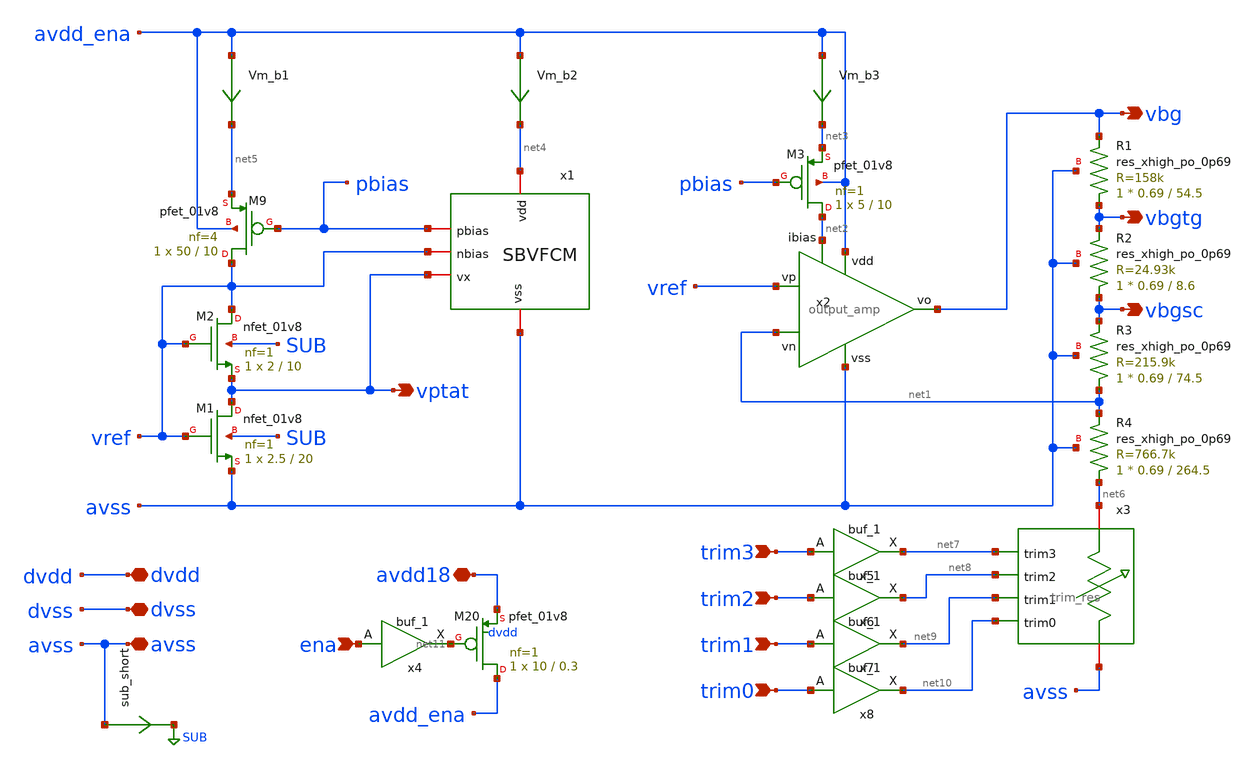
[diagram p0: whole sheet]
** sch_path: xschem/sky130_ak_ip__cmos_vref.sch
**.subckt sky130_ak_ip__cmos_vref vbg avss avdd18 dvdd dvss ena vbgsc vbgtg trim3 trim2 trim1 trim0
*+ vptat
*.opin vbg
*.iopin avss
*.iopin avdd18
*.iopin dvdd
*.iopin dvss
*.ipin ena
*.opin vbgsc
*.opin vbgtg
*.ipin trim3
*.ipin trim2
*.ipin trim1
*.ipin trim0
*.opin vptat
XM2 vref vref vptat SUB sky130_fd_pr__nfet_01v8 L=10 W=2 nf=1 ad='int((nf+1)/2) * W/nf * 0.29' as='int((nf+2)/2) * W/nf * 0.29'
+ pd='2*int((nf+1)/2) * (W/nf + 0.29)' ps='2*int((nf+2)/2) * (W/nf + 0.29)' nrd='0.29 / W' nrs='0.29 / W'
+ sa=0 sb=0 sd=0 mult=1 m=1
XM1 vptat vref avss SUB sky130_fd_pr__nfet_01v8 L=20 W=2.5 nf=1 ad='int((nf+1)/2) * W/nf * 0.29' as='int((nf+2)/2) * W/nf * 0.29'
+ pd='2*int((nf+1)/2) * (W/nf + 0.29)' ps='2*int((nf+2)/2) * (W/nf + 0.29)' nrd='0.29 / W' nrs='0.29 / W'
+ sa=0 sb=0 sd=0 mult=1 m=1
XM9 vref pbias net5 avdd_ena sky130_fd_pr__pfet_01v8 L=10 W=50 nf=4 ad='int((nf+1)/2) * W/nf * 0.29'
+ as='int((nf+2)/2) * W/nf * 0.29' pd='2*int((nf+1)/2) * (W/nf + 0.29)' ps='2*int((nf+2)/2) * (W/nf + 0.29)'
+ nrd='0.29 / W' nrs='0.29 / W' sa=0 sb=0 sd=0 mult=1 m=1
XM20 avdd_ena net11 avdd18 dvdd sky130_fd_pr__pfet_01v8 L=0.3 W=10 nf=1 ad='int((nf+1)/2) * W/nf * 0.29'
+ as='int((nf+2)/2) * W/nf * 0.29' pd='2*int((nf+1)/2) * (W/nf + 0.29)' ps='2*int((nf+2)/2) * (W/nf + 0.29)'
+ nrd='0.29 / W' nrs='0.29 / W' sa=0 sb=0 sd=0 mult=1 m=1
x1 net4 pbias vref vptat avss sbvfcm
x2 avdd_ena vbg vref net1 net2 avss output_amp
XM3 net2 pbias net3 avdd_ena sky130_fd_pr__pfet_01v8 L=10 W=5 nf=1 ad='int((nf+1)/2) * W/nf * 0.29' as='int((nf+2)/2) * W/nf * 0.29'
+ pd='2*int((nf+1)/2) * (W/nf + 0.29)' ps='2*int((nf+2)/2) * (W/nf + 0.29)' nrd='0.29 / W' nrs='0.29 / W'
+ sa=0 sb=0 sd=0 mult=1 m=1
Vm_b1 avdd_ena net5 0
.save i(vm_b1)
Vm_b2 avdd_ena net4 0
.save i(vm_b2)
Vm_b3 avdd_ena net3 0
.save i(vm_b3)
x3 net6 net10 net8 net7 net9 avss trim_res
XR4 net6 net1 avss sky130_fd_pr__res_xhigh_po_0p69 L=264.5 mult=1 m=1
XR3 net1 vbgsc avss sky130_fd_pr__res_xhigh_po_0p69 L=74.5 mult=1 m=1
XR2 vbgsc vbgtg avss sky130_fd_pr__res_xhigh_po_0p69 L=8.6 mult=1 m=1
XR1 vbgtg vbg avss sky130_fd_pr__res_xhigh_po_0p69 L=54.5 mult=1 m=1
sub_short avss SUB 0
.save i(sub_short)
x4 ena dvss SUB dvdd dvdd net11 sky130_fd_sc_hd__buf_1
x5 trim3 dvss SUB dvdd dvdd net7 sky130_fd_sc_hd__buf_1
x6 trim2 dvss SUB dvdd dvdd net8 sky130_fd_sc_hd__buf_1
x7 trim1 dvss SUB dvdd dvdd net9 sky130_fd_sc_hd__buf_1
x8 trim0 dvss SUB dvdd dvdd net10 sky130_fd_sc_hd__buf_1
**.ends

* expanding   symbol:  /home/moduhub/work/sky130_ak_ip__cmos_vref/xschem/sbvfcm.sym # of pins=5
** sym_path: /home/moduhub/work/sky130_ak_ip__cmos_vref/xschem/sbvfcm.sym
** sch_path: /home/moduhub/work/sky130_ak_ip__cmos_vref/xschem/sbvfcm.sch
.subckt sbvfcm vdd pbias nbias vx vss
*.iopin vss
*.iopin vdd
*.iopin vx
*.iopin pbias
*.iopin nbias
XM3 net1 vbias_st vx vss sky130_fd_pr__nfet_01v8 L=2 W=100 nf=8 ad='int((nf+1)/2) * W/nf * 0.29' as='int((nf+2)/2) * W/nf * 0.29'
+ pd='2*int((nf+1)/2) * (W/nf + 0.29)' ps='2*int((nf+2)/2) * (W/nf + 0.29)' nrd='0.29 / W' nrs='0.29 / W'
+ sa=0 sb=0 sd=0 mult=1 m=1
XM4 net2 vbias_st vss vss sky130_fd_pr__nfet_01v8 L=2 W=5 nf=1 ad='int((nf+1)/2) * W/nf * 0.29' as='int((nf+2)/2) * W/nf * 0.29'
+ pd='2*int((nf+1)/2) * (W/nf + 0.29)' ps='2*int((nf+2)/2) * (W/nf + 0.29)' nrd='0.29 / W' nrs='0.29 / W'
+ sa=0 sb=0 sd=0 mult=1 m=1
XM5 pbias nbias net1 vss sky130_fd_pr__nfet_01v8 L=10 W=10 nf=1 ad='int((nf+1)/2) * W/nf * 0.29' as='int((nf+2)/2) * W/nf * 0.29'
+ pd='2*int((nf+1)/2) * (W/nf + 0.29)' ps='2*int((nf+2)/2) * (W/nf + 0.29)' nrd='0.29 / W' nrs='0.29 / W'
+ sa=0 sb=0 sd=0 mult=1 m=1
XM6 vbias_st nbias net2 vss sky130_fd_pr__nfet_01v8 L=10 W=10 nf=1 ad='int((nf+1)/2) * W/nf * 0.29' as='int((nf+2)/2) * W/nf * 0.29'
+ pd='2*int((nf+1)/2) * (W/nf + 0.29)' ps='2*int((nf+2)/2) * (W/nf + 0.29)' nrd='0.29 / W' nrs='0.29 / W'
+ sa=0 sb=0 sd=0 mult=1 m=1
XM7 pbias pbias net6 vdd sky130_fd_pr__pfet_01v8 L=10 W=5 nf=1 ad='int((nf+1)/2) * W/nf * 0.29' as='int((nf+2)/2) * W/nf * 0.29'
+ pd='2*int((nf+1)/2) * (W/nf + 0.29)' ps='2*int((nf+2)/2) * (W/nf + 0.29)' nrd='0.29 / W' nrs='0.29 / W'
+ sa=0 sb=0 sd=0 mult=1 m=1
XM8 vbias_st pbias net7 vdd sky130_fd_pr__pfet_01v8 L=10 W=5 nf=1 ad='int((nf+1)/2) * W/nf * 0.29' as='int((nf+2)/2) * W/nf * 0.29'
+ pd='2*int((nf+1)/2) * (W/nf + 0.29)' ps='2*int((nf+2)/2) * (W/nf + 0.29)' nrd='0.29 / W' nrs='0.29 / W'
+ sa=0 sb=0 sd=0 mult=1 m=1
XM10 net4 net3 vss vss sky130_fd_pr__nfet_01v8 L=10 W=5 nf=1 ad='int((nf+1)/2) * W/nf * 0.29' as='int((nf+2)/2) * W/nf * 0.29'
+ pd='2*int((nf+1)/2) * (W/nf + 0.29)' ps='2*int((nf+2)/2) * (W/nf + 0.29)' nrd='0.29 / W' nrs='0.29 / W'
+ sa=0 sb=0 sd=0 mult=1 m=1
XM11 net3 vbias_st vss vss sky130_fd_pr__nfet_01v8 L=5 W=10 nf=1 ad='int((nf+1)/2) * W/nf * 0.29' as='int((nf+2)/2) * W/nf * 0.29'
+ pd='2*int((nf+1)/2) * (W/nf + 0.29)' ps='2*int((nf+2)/2) * (W/nf + 0.29)' nrd='0.29 / W' nrs='0.29 / W'
+ sa=0 sb=0 sd=0 mult=1 m=1
XC1 net5 net3 sky130_fd_pr__cap_mim_m3_1 W=5 L=5 MF=2 m=2
Vm_st1 pbias net4 0
.save i(vm_st1)
Vm_st2 vdd net5 0
.save i(vm_st2)
Vm_b1 vdd net6 0
.save i(vm_b1)
Vm_b2 vdd net7 0
.save i(vm_b2)
.ends


* expanding   symbol:  /home/moduhub/work/sky130_ak_ip__cmos_vref/xschem/output_amp.sym # of pins=6
** sym_path: /home/moduhub/work/sky130_ak_ip__cmos_vref/xschem/output_amp.sym
** sch_path: /home/moduhub/work/sky130_ak_ip__cmos_vref/xschem/output_amp.sch
.subckt output_amp vdd vo vp vn ibias vss
*.ipin vp
*.ipin vn
*.ipin ibias
*.opin vo
*.ipin vss
*.ipin vdd
XM1 ibias ibias vss vss sky130_fd_pr__nfet_01v8 L=1 W=2.5 nf=1 ad='int((nf+1)/2) * W/nf * 0.29' as='int((nf+2)/2) * W/nf * 0.29'
+ pd='2*int((nf+1)/2) * (W/nf + 0.29)' ps='2*int((nf+2)/2) * (W/nf + 0.29)' nrd='0.29 / W' nrs='0.29 / W'
+ sa=0 sb=0 sd=0 mult=1 m=1
XM2 net2 ibias vss vss sky130_fd_pr__nfet_01v8 L=1 W=5 nf=1 ad='int((nf+1)/2) * W/nf * 0.29' as='int((nf+2)/2) * W/nf * 0.29'
+ pd='2*int((nf+1)/2) * (W/nf + 0.29)' ps='2*int((nf+2)/2) * (W/nf + 0.29)' nrd='0.29 / W' nrs='0.29 / W'
+ sa=0 sb=0 sd=0 mult=1 m=1
XM7 vo_pre net1 net4 vdd sky130_fd_pr__pfet_01v8 L=10 W=5 nf=1 ad='int((nf+1)/2) * W/nf * 0.29' as='int((nf+2)/2) * W/nf * 0.29'
+ pd='2*int((nf+1)/2) * (W/nf + 0.29)' ps='2*int((nf+2)/2) * (W/nf + 0.29)' nrd='0.29 / W' nrs='0.29 / W'
+ sa=0 sb=0 sd=0 mult=1 m=1
XM4 net7 vn vcm vss sky130_fd_pr__nfet_01v8 L=2 W=10 nf=2 ad='int((nf+1)/2) * W/nf * 0.29' as='int((nf+2)/2) * W/nf * 0.29'
+ pd='2*int((nf+1)/2) * (W/nf + 0.29)' ps='2*int((nf+2)/2) * (W/nf + 0.29)' nrd='0.29 / W' nrs='0.29 / W'
+ sa=0 sb=0 sd=0 mult=1 m=1
XM5 net8 vp vcm vss sky130_fd_pr__nfet_01v8 L=2 W=10 nf=2 ad='int((nf+1)/2) * W/nf * 0.29' as='int((nf+2)/2) * W/nf * 0.29'
+ pd='2*int((nf+1)/2) * (W/nf + 0.29)' ps='2*int((nf+2)/2) * (W/nf + 0.29)' nrd='0.29 / W' nrs='0.29 / W'
+ sa=0 sb=0 sd=0 mult=1 m=1
XM6 net1 net1 net3 vdd sky130_fd_pr__pfet_01v8 L=10 W=5 nf=1 ad='int((nf+1)/2) * W/nf * 0.29' as='int((nf+2)/2) * W/nf * 0.29'
+ pd='2*int((nf+1)/2) * (W/nf + 0.29)' ps='2*int((nf+2)/2) * (W/nf + 0.29)' nrd='0.29 / W' nrs='0.29 / W'
+ sa=0 sb=0 sd=0 mult=1 m=1
Vm_b1 vdd net3 0
.save i(vm_b1)
XM3 net6 ibias vss vss sky130_fd_pr__nfet_01v8 L=1 W=8 nf=1 ad='int((nf+1)/2) * W/nf * 0.29' as='int((nf+2)/2) * W/nf * 0.29'
+ pd='2*int((nf+1)/2) * (W/nf + 0.29)' ps='2*int((nf+2)/2) * (W/nf + 0.29)' nrd='0.29 / W' nrs='0.29 / W'
+ sa=0 sb=0 sd=0 mult=1 m=1
XM8 vo vo_pre net5 vdd sky130_fd_pr__pfet_01v8 L=5 W=40 nf=2 ad='int((nf+1)/2) * W/nf * 0.29' as='int((nf+2)/2) * W/nf * 0.29'
+ pd='2*int((nf+1)/2) * (W/nf + 0.29)' ps='2*int((nf+2)/2) * (W/nf + 0.29)' nrd='0.29 / W' nrs='0.29 / W'
+ sa=0 sb=0 sd=0 mult=1 m=1
Vm_op vdd net5 0
.save i(vm_op)
Vm_cm vcm net2 0
.save i(vm_cm)
Vm_b2 vdd net4 0
.save i(vm_b2)
XC2 vo vo_pre sky130_fd_pr__cap_mim_m3_1 W=5 L=5 MF=10 m=10
Vm_on vo net6 0
.save i(vm_on)
XM9 net1 vn net7 vss sky130_fd_pr__nfet_05v0_nvt L=2 W=20 nf=2 ad='int((nf+1)/2) * W/nf * 0.29' as='int((nf+2)/2) * W/nf * 0.29'
+ pd='2*int((nf+1)/2) * (W/nf + 0.29)' ps='2*int((nf+2)/2) * (W/nf + 0.29)' nrd='0.29 / W' nrs='0.29 / W'
+ sa=0 sb=0 sd=0 mult=1 m=1
XM10 vo_pre vp net8 vss sky130_fd_pr__nfet_05v0_nvt L=2 W=20 nf=2 ad='int((nf+1)/2) * W/nf * 0.29' as='int((nf+2)/2) * W/nf * 0.29'
+ pd='2*int((nf+1)/2) * (W/nf + 0.29)' ps='2*int((nf+2)/2) * (W/nf + 0.29)' nrd='0.29 / W' nrs='0.29 / W'
+ sa=0 sb=0 sd=0 mult=1 m=1
.ends


* expanding   symbol:  /home/moduhub/work/sky130_ak_ip__cmos_vref/xschem/trim_res.sym # of pins=6
** sym_path: xschem/trim_res.sym
** sch_path: xschem/trim_res.sch
.subckt trim_res A trim0 trim2 trim3 trim1 B
*.ipin trim0
*.ipin trim1
*.ipin trim2
*.ipin trim3
*.iopin B
*.iopin A
XM1 A trim3 net3 SUB sky130_fd_pr__nfet_01v8 L=2 W=10 nf=1 ad='int((nf+1)/2) * W/nf * 0.29' as='int((nf+2)/2) * W/nf * 0.29'
+ pd='2*int((nf+1)/2) * (W/nf + 0.29)' ps='2*int((nf+2)/2) * (W/nf + 0.29)' nrd='0.29 / W' nrs='0.29 / W'
+ sa=0 sb=0 sd=0 mult=1 m=1
XM2 net3 trim2 net2 SUB sky130_fd_pr__nfet_01v8 L=2 W=10 nf=1 ad='int((nf+1)/2) * W/nf * 0.29' as='int((nf+2)/2) * W/nf * 0.29'
+ pd='2*int((nf+1)/2) * (W/nf + 0.29)' ps='2*int((nf+2)/2) * (W/nf + 0.29)' nrd='0.29 / W' nrs='0.29 / W'
+ sa=0 sb=0 sd=0 mult=1 m=1
XM3 net2 trim1 net1 SUB sky130_fd_pr__nfet_01v8 L=2 W=10 nf=1 ad='int((nf+1)/2) * W/nf * 0.29' as='int((nf+2)/2) * W/nf * 0.29'
+ pd='2*int((nf+1)/2) * (W/nf + 0.29)' ps='2*int((nf+2)/2) * (W/nf + 0.29)' nrd='0.29 / W' nrs='0.29 / W'
+ sa=0 sb=0 sd=0 mult=1 m=1
XM4 net1 trim0 B SUB sky130_fd_pr__nfet_01v8 L=2 W=10 nf=1 ad='int((nf+1)/2) * W/nf * 0.29' as='int((nf+2)/2) * W/nf * 0.29'
+ pd='2*int((nf+1)/2) * (W/nf + 0.29)' ps='2*int((nf+2)/2) * (W/nf + 0.29)' nrd='0.29 / W' nrs='0.29 / W'
+ sa=0 sb=0 sd=0 mult=1 m=1
XR1 B net1 SUB sky130_fd_pr__res_xhigh_po_0p69 L=3.45 mult=1 m=1
XR2 net1 net2 SUB sky130_fd_pr__res_xhigh_po_0p69 L=6.9 mult=1 m=1
XR3 net2 net3 SUB sky130_fd_pr__res_xhigh_po_0p69 L=13.8 mult=1 m=1
XR4 net3 A SUB sky130_fd_pr__res_xhigh_po_0p69 L=27.6 mult=1 m=1
.ends

.GLOBAL SUB
.end
